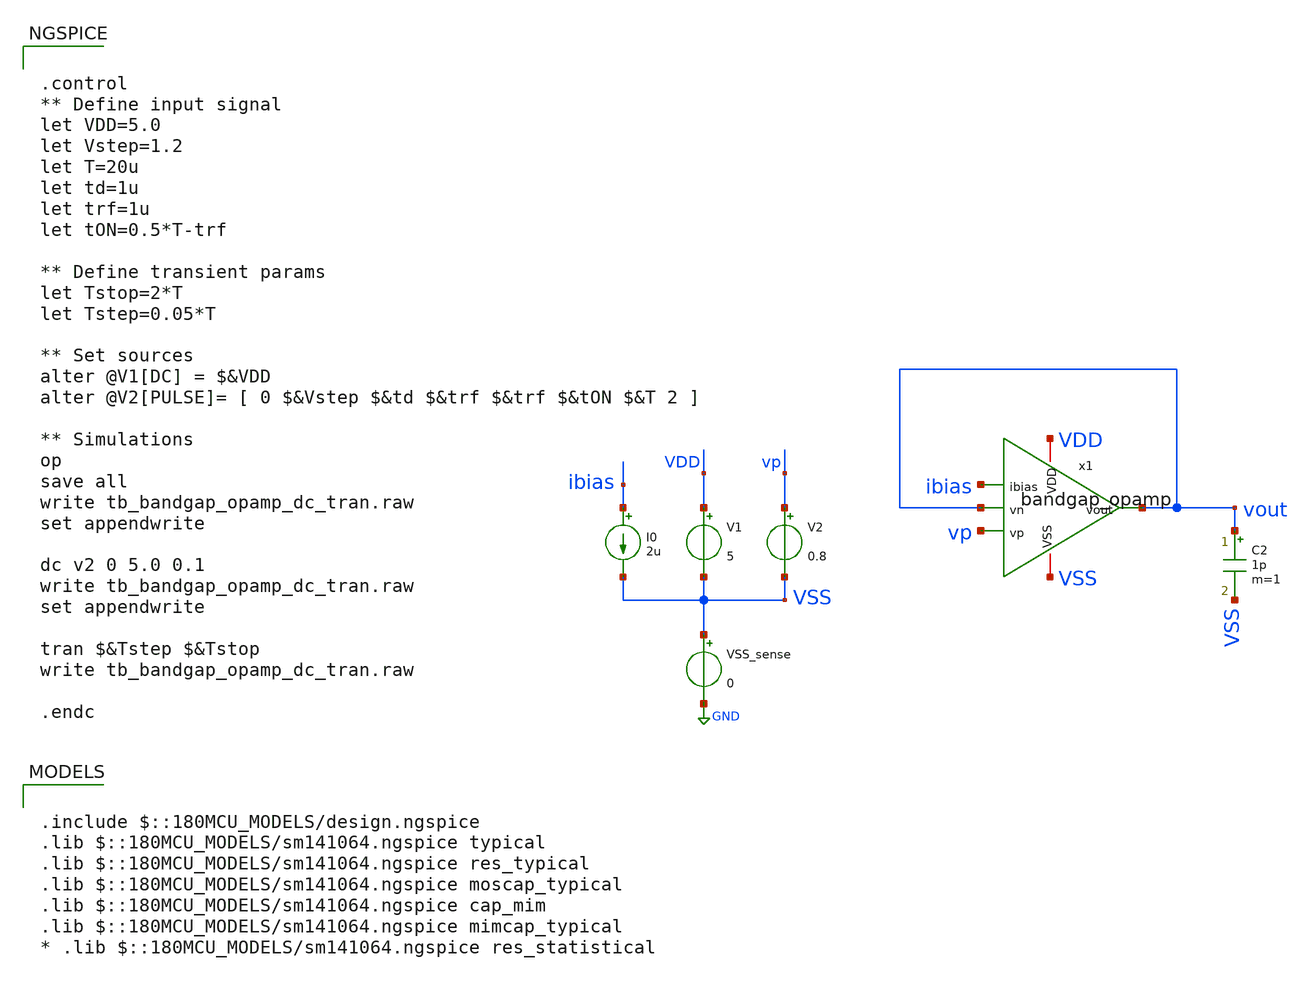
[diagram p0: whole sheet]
** sch_path: designs/libs/tb_bandgap/tb_bandgap_opamp_dc_tran/tb_bandgap_opamp_dc_tran.sch
**.subckt tb_bandgap_opamp_dc_tran
V1 VDD VSS 5
V2 vp VSS 0.8
VSS_sense VSS GND 0
C2 vout VSS 1p m=1
I0 ibias VSS 2u
x1 VDD ibias vout vp vout VSS bandgap_opamp
**** begin user architecture code

.include $::180MCU_MODELS/design.ngspice
.lib $::180MCU_MODELS/sm141064.ngspice typical
.lib $::180MCU_MODELS/sm141064.ngspice res_typical
.lib $::180MCU_MODELS/sm141064.ngspice moscap_typical
.lib $::180MCU_MODELS/sm141064.ngspice cap_mim
.lib $::180MCU_MODELS/sm141064.ngspice mimcap_typical
* .lib $::180MCU_MODELS/sm141064.ngspice res_statistical



.control
** Define input signal
let VDD=5.0
let Vstep=1.2
let T=20u
let td=1u
let trf=1u
let tON=0.5*T-trf

** Define transient params
let Tstop=2*T
let Tstep=0.05*T

** Set sources
alter @V1[DC] = $&VDD
alter @V2[PULSE]= [ 0 $&Vstep $&td $&trf $&trf $&tON $&T 2 ]

** Simulations
op
save all
write tb_bandgap_opamp_dc_tran.raw
set appendwrite

dc v2 0 5.0 0.1
write tb_bandgap_opamp_dc_tran.raw
set appendwrite

tran $&Tstep $&Tstop
write tb_bandgap_opamp_dc_tran.raw

.endc


**** end user architecture code
**.ends

* expanding   symbol:  libs/core_bandgap/bandgap_opamp/bandgap_opamp.sym # of pins=6
** sym_path: designs/libs/core_bandgap/bandgap_opamp/bandgap_opamp.sym
** sch_path: designs/libs/core_bandgap/bandgap_opamp/bandgap_opamp.sch
.subckt bandgap_opamp VDD ibias vn vp vout VSS
*.ipin vn
*.ipin vp
*.opin vout
*.ipin ibias
*.iopin VDD
*.iopin VSS
XMpref0 ibias ibias VDD VDD pfet_05v0 L=1u W=0.5u nf=1 ad='int((nf+1)/2) * W/nf * 0.18u' as='int((nf+2)/2) * W/nf * 0.18u'
+ pd='2*int((nf+1)/2) * (W/nf + 0.18u)' ps='2*int((nf+2)/2) * (W/nf + 0.18u)' nrd='0.18u / W' nrs='0.18u / W'
+ sa=0 sb=0 sd=0 m=2
XMnload0 vnload vnload VSS VSS nfet_05v0 L=2u W=0.5u nf=1 ad='int((nf+1)/2) * W/nf * 0.18u' as='int((nf+2)/2) * W/nf * 0.18u'
+ pd='2*int((nf+1)/2) * (W/nf + 0.18u)' ps='2*int((nf+2)/2) * (W/nf + 0.18u)' nrd='0.18u / W' nrs='0.18u / W'
+ sa=0 sb=0 sd=0 m=2
XMpref1 vptail ibias VDD VDD pfet_05v0 L=1u W=0.5u nf=1 ad='int((nf+1)/2) * W/nf * 0.18u' as='int((nf+2)/2) * W/nf * 0.18u'
+ pd='2*int((nf+1)/2) * (W/nf + 0.18u)' ps='2*int((nf+2)/2) * (W/nf + 0.18u)' nrd='0.18u / W' nrs='0.18u / W'
+ sa=0 sb=0 sd=0 m=2
XMpref2 vout ibias VDD VDD pfet_05v0 L=1u W=0.5u nf=1 ad='int((nf+1)/2) * W/nf * 0.18u' as='int((nf+2)/2) * W/nf * 0.18u'
+ pd='2*int((nf+1)/2) * (W/nf + 0.18u)' ps='2*int((nf+2)/2) * (W/nf + 0.18u)' nrd='0.18u / W' nrs='0.18u / W'
+ sa=0 sb=0 sd=0 m=8
XMpdiff0 vnload vn vptail VDD pfet_05v0 L=1u W=2u nf=1 ad='int((nf+1)/2) * W/nf * 0.18u' as='int((nf+2)/2) * W/nf * 0.18u'
+ pd='2*int((nf+1)/2) * (W/nf + 0.18u)' ps='2*int((nf+2)/2) * (W/nf + 0.18u)' nrd='0.18u / W' nrs='0.18u / W'
+ sa=0 sb=0 sd=0 m=2
XMpdiff1 vout_1st vp vptail VDD pfet_05v0 L=1u W=2u nf=1 ad='int((nf+1)/2) * W/nf * 0.18u' as='int((nf+2)/2) * W/nf * 0.18u'
+ pd='2*int((nf+1)/2) * (W/nf + 0.18u)' ps='2*int((nf+2)/2) * (W/nf + 0.18u)' nrd='0.18u / W' nrs='0.18u / W'
+ sa=0 sb=0 sd=0 m=2
XMnload1 vout_1st vnload VSS VSS nfet_05v0 L=2u W=0.5u nf=1 ad='int((nf+1)/2) * W/nf * 0.18u' as='int((nf+2)/2) * W/nf * 0.18u'
+ pd='2*int((nf+1)/2) * (W/nf + 0.18u)' ps='2*int((nf+2)/2) * (W/nf + 0.18u)' nrd='0.18u / W' nrs='0.18u / W'
+ sa=0 sb=0 sd=0 m=2
XMncs vout vout_1st VSS VSS nfet_05v0 L=2u W=0.5u nf=1 ad='int((nf+1)/2) * W/nf * 0.18u' as='int((nf+2)/2) * W/nf * 0.18u'
+ pd='2*int((nf+1)/2) * (W/nf + 0.18u)' ps='2*int((nf+2)/2) * (W/nf + 0.18u)' nrd='0.18u / W' nrs='0.18u / W'
+ sa=0 sb=0 sd=0 m=16
XMpref_dumm_L[3] VDD VDD VDD VDD pfet_05v0 L=1u W=0.5u nf=1 ad='int((nf+1)/2) * W/nf * 0.18u' as='int((nf+2)/2) * W/nf * 0.18u'
+ pd='2*int((nf+1)/2) * (W/nf + 0.18u)' ps='2*int((nf+2)/2) * (W/nf + 0.18u)' nrd='0.18u / W' nrs='0.18u / W'
+ sa=0 sb=0 sd=0 m=1
XMpref_dumm_L[2] VDD VDD VDD VDD pfet_05v0 L=1u W=0.5u nf=1 ad='int((nf+1)/2) * W/nf * 0.18u' as='int((nf+2)/2) * W/nf * 0.18u'
+ pd='2*int((nf+1)/2) * (W/nf + 0.18u)' ps='2*int((nf+2)/2) * (W/nf + 0.18u)' nrd='0.18u / W' nrs='0.18u / W'
+ sa=0 sb=0 sd=0 m=1
XMpref_dumm_L[1] VDD VDD VDD VDD pfet_05v0 L=1u W=0.5u nf=1 ad='int((nf+1)/2) * W/nf * 0.18u' as='int((nf+2)/2) * W/nf * 0.18u'
+ pd='2*int((nf+1)/2) * (W/nf + 0.18u)' ps='2*int((nf+2)/2) * (W/nf + 0.18u)' nrd='0.18u / W' nrs='0.18u / W'
+ sa=0 sb=0 sd=0 m=1
XMpref_dumm_L[0] VDD VDD VDD VDD pfet_05v0 L=1u W=0.5u nf=1 ad='int((nf+1)/2) * W/nf * 0.18u' as='int((nf+2)/2) * W/nf * 0.18u'
+ pd='2*int((nf+1)/2) * (W/nf + 0.18u)' ps='2*int((nf+2)/2) * (W/nf + 0.18u)' nrd='0.18u / W' nrs='0.18u / W'
+ sa=0 sb=0 sd=0 m=1
XMpref_dumm_TP[23] VDD VDD VDD VDD pfet_05v0 L=1u W=0.5u nf=1 ad='int((nf+1)/2) * W/nf * 0.18u' as='int((nf+2)/2) * W/nf * 0.18u'
+ pd='2*int((nf+1)/2) * (W/nf + 0.18u)' ps='2*int((nf+2)/2) * (W/nf + 0.18u)' nrd='0.18u / W' nrs='0.18u / W'
+ sa=0 sb=0 sd=0 m=1
XMpref_dumm_TP[22] VDD VDD VDD VDD pfet_05v0 L=1u W=0.5u nf=1 ad='int((nf+1)/2) * W/nf * 0.18u' as='int((nf+2)/2) * W/nf * 0.18u'
+ pd='2*int((nf+1)/2) * (W/nf + 0.18u)' ps='2*int((nf+2)/2) * (W/nf + 0.18u)' nrd='0.18u / W' nrs='0.18u / W'
+ sa=0 sb=0 sd=0 m=1
XMpref_dumm_TP[21] VDD VDD VDD VDD pfet_05v0 L=1u W=0.5u nf=1 ad='int((nf+1)/2) * W/nf * 0.18u' as='int((nf+2)/2) * W/nf * 0.18u'
+ pd='2*int((nf+1)/2) * (W/nf + 0.18u)' ps='2*int((nf+2)/2) * (W/nf + 0.18u)' nrd='0.18u / W' nrs='0.18u / W'
+ sa=0 sb=0 sd=0 m=1
XMpref_dumm_TP[20] VDD VDD VDD VDD pfet_05v0 L=1u W=0.5u nf=1 ad='int((nf+1)/2) * W/nf * 0.18u' as='int((nf+2)/2) * W/nf * 0.18u'
+ pd='2*int((nf+1)/2) * (W/nf + 0.18u)' ps='2*int((nf+2)/2) * (W/nf + 0.18u)' nrd='0.18u / W' nrs='0.18u / W'
+ sa=0 sb=0 sd=0 m=1
XMpref_dumm_TP[19] VDD VDD VDD VDD pfet_05v0 L=1u W=0.5u nf=1 ad='int((nf+1)/2) * W/nf * 0.18u' as='int((nf+2)/2) * W/nf * 0.18u'
+ pd='2*int((nf+1)/2) * (W/nf + 0.18u)' ps='2*int((nf+2)/2) * (W/nf + 0.18u)' nrd='0.18u / W' nrs='0.18u / W'
+ sa=0 sb=0 sd=0 m=1
XMpref_dumm_TP[18] VDD VDD VDD VDD pfet_05v0 L=1u W=0.5u nf=1 ad='int((nf+1)/2) * W/nf * 0.18u' as='int((nf+2)/2) * W/nf * 0.18u'
+ pd='2*int((nf+1)/2) * (W/nf + 0.18u)' ps='2*int((nf+2)/2) * (W/nf + 0.18u)' nrd='0.18u / W' nrs='0.18u / W'
+ sa=0 sb=0 sd=0 m=1
XMpref_dumm_TP[17] VDD VDD VDD VDD pfet_05v0 L=1u W=0.5u nf=1 ad='int((nf+1)/2) * W/nf * 0.18u' as='int((nf+2)/2) * W/nf * 0.18u'
+ pd='2*int((nf+1)/2) * (W/nf + 0.18u)' ps='2*int((nf+2)/2) * (W/nf + 0.18u)' nrd='0.18u / W' nrs='0.18u / W'
+ sa=0 sb=0 sd=0 m=1
XMpref_dumm_TP[16] VDD VDD VDD VDD pfet_05v0 L=1u W=0.5u nf=1 ad='int((nf+1)/2) * W/nf * 0.18u' as='int((nf+2)/2) * W/nf * 0.18u'
+ pd='2*int((nf+1)/2) * (W/nf + 0.18u)' ps='2*int((nf+2)/2) * (W/nf + 0.18u)' nrd='0.18u / W' nrs='0.18u / W'
+ sa=0 sb=0 sd=0 m=1
XMpref_dumm_TP[15] VDD VDD VDD VDD pfet_05v0 L=1u W=0.5u nf=1 ad='int((nf+1)/2) * W/nf * 0.18u' as='int((nf+2)/2) * W/nf * 0.18u'
+ pd='2*int((nf+1)/2) * (W/nf + 0.18u)' ps='2*int((nf+2)/2) * (W/nf + 0.18u)' nrd='0.18u / W' nrs='0.18u / W'
+ sa=0 sb=0 sd=0 m=1
XMpref_dumm_TP[14] VDD VDD VDD VDD pfet_05v0 L=1u W=0.5u nf=1 ad='int((nf+1)/2) * W/nf * 0.18u' as='int((nf+2)/2) * W/nf * 0.18u'
+ pd='2*int((nf+1)/2) * (W/nf + 0.18u)' ps='2*int((nf+2)/2) * (W/nf + 0.18u)' nrd='0.18u / W' nrs='0.18u / W'
+ sa=0 sb=0 sd=0 m=1
XMpref_dumm_TP[13] VDD VDD VDD VDD pfet_05v0 L=1u W=0.5u nf=1 ad='int((nf+1)/2) * W/nf * 0.18u' as='int((nf+2)/2) * W/nf * 0.18u'
+ pd='2*int((nf+1)/2) * (W/nf + 0.18u)' ps='2*int((nf+2)/2) * (W/nf + 0.18u)' nrd='0.18u / W' nrs='0.18u / W'
+ sa=0 sb=0 sd=0 m=1
XMpref_dumm_TP[12] VDD VDD VDD VDD pfet_05v0 L=1u W=0.5u nf=1 ad='int((nf+1)/2) * W/nf * 0.18u' as='int((nf+2)/2) * W/nf * 0.18u'
+ pd='2*int((nf+1)/2) * (W/nf + 0.18u)' ps='2*int((nf+2)/2) * (W/nf + 0.18u)' nrd='0.18u / W' nrs='0.18u / W'
+ sa=0 sb=0 sd=0 m=1
XMpref_dumm_TP[11] VDD VDD VDD VDD pfet_05v0 L=1u W=0.5u nf=1 ad='int((nf+1)/2) * W/nf * 0.18u' as='int((nf+2)/2) * W/nf * 0.18u'
+ pd='2*int((nf+1)/2) * (W/nf + 0.18u)' ps='2*int((nf+2)/2) * (W/nf + 0.18u)' nrd='0.18u / W' nrs='0.18u / W'
+ sa=0 sb=0 sd=0 m=1
XMpref_dumm_TP[10] VDD VDD VDD VDD pfet_05v0 L=1u W=0.5u nf=1 ad='int((nf+1)/2) * W/nf * 0.18u' as='int((nf+2)/2) * W/nf * 0.18u'
+ pd='2*int((nf+1)/2) * (W/nf + 0.18u)' ps='2*int((nf+2)/2) * (W/nf + 0.18u)' nrd='0.18u / W' nrs='0.18u / W'
+ sa=0 sb=0 sd=0 m=1
XMpref_dumm_TP[9] VDD VDD VDD VDD pfet_05v0 L=1u W=0.5u nf=1 ad='int((nf+1)/2) * W/nf * 0.18u' as='int((nf+2)/2) * W/nf * 0.18u'
+ pd='2*int((nf+1)/2) * (W/nf + 0.18u)' ps='2*int((nf+2)/2) * (W/nf + 0.18u)' nrd='0.18u / W' nrs='0.18u / W'
+ sa=0 sb=0 sd=0 m=1
XMpref_dumm_TP[8] VDD VDD VDD VDD pfet_05v0 L=1u W=0.5u nf=1 ad='int((nf+1)/2) * W/nf * 0.18u' as='int((nf+2)/2) * W/nf * 0.18u'
+ pd='2*int((nf+1)/2) * (W/nf + 0.18u)' ps='2*int((nf+2)/2) * (W/nf + 0.18u)' nrd='0.18u / W' nrs='0.18u / W'
+ sa=0 sb=0 sd=0 m=1
XMpref_dumm_TP[7] VDD VDD VDD VDD pfet_05v0 L=1u W=0.5u nf=1 ad='int((nf+1)/2) * W/nf * 0.18u' as='int((nf+2)/2) * W/nf * 0.18u'
+ pd='2*int((nf+1)/2) * (W/nf + 0.18u)' ps='2*int((nf+2)/2) * (W/nf + 0.18u)' nrd='0.18u / W' nrs='0.18u / W'
+ sa=0 sb=0 sd=0 m=1
XMpref_dumm_TP[6] VDD VDD VDD VDD pfet_05v0 L=1u W=0.5u nf=1 ad='int((nf+1)/2) * W/nf * 0.18u' as='int((nf+2)/2) * W/nf * 0.18u'
+ pd='2*int((nf+1)/2) * (W/nf + 0.18u)' ps='2*int((nf+2)/2) * (W/nf + 0.18u)' nrd='0.18u / W' nrs='0.18u / W'
+ sa=0 sb=0 sd=0 m=1
XMpref_dumm_TP[5] VDD VDD VDD VDD pfet_05v0 L=1u W=0.5u nf=1 ad='int((nf+1)/2) * W/nf * 0.18u' as='int((nf+2)/2) * W/nf * 0.18u'
+ pd='2*int((nf+1)/2) * (W/nf + 0.18u)' ps='2*int((nf+2)/2) * (W/nf + 0.18u)' nrd='0.18u / W' nrs='0.18u / W'
+ sa=0 sb=0 sd=0 m=1
XMpref_dumm_TP[4] VDD VDD VDD VDD pfet_05v0 L=1u W=0.5u nf=1 ad='int((nf+1)/2) * W/nf * 0.18u' as='int((nf+2)/2) * W/nf * 0.18u'
+ pd='2*int((nf+1)/2) * (W/nf + 0.18u)' ps='2*int((nf+2)/2) * (W/nf + 0.18u)' nrd='0.18u / W' nrs='0.18u / W'
+ sa=0 sb=0 sd=0 m=1
XMpref_dumm_TP[3] VDD VDD VDD VDD pfet_05v0 L=1u W=0.5u nf=1 ad='int((nf+1)/2) * W/nf * 0.18u' as='int((nf+2)/2) * W/nf * 0.18u'
+ pd='2*int((nf+1)/2) * (W/nf + 0.18u)' ps='2*int((nf+2)/2) * (W/nf + 0.18u)' nrd='0.18u / W' nrs='0.18u / W'
+ sa=0 sb=0 sd=0 m=1
XMpref_dumm_TP[2] VDD VDD VDD VDD pfet_05v0 L=1u W=0.5u nf=1 ad='int((nf+1)/2) * W/nf * 0.18u' as='int((nf+2)/2) * W/nf * 0.18u'
+ pd='2*int((nf+1)/2) * (W/nf + 0.18u)' ps='2*int((nf+2)/2) * (W/nf + 0.18u)' nrd='0.18u / W' nrs='0.18u / W'
+ sa=0 sb=0 sd=0 m=1
XMpref_dumm_TP[1] VDD VDD VDD VDD pfet_05v0 L=1u W=0.5u nf=1 ad='int((nf+1)/2) * W/nf * 0.18u' as='int((nf+2)/2) * W/nf * 0.18u'
+ pd='2*int((nf+1)/2) * (W/nf + 0.18u)' ps='2*int((nf+2)/2) * (W/nf + 0.18u)' nrd='0.18u / W' nrs='0.18u / W'
+ sa=0 sb=0 sd=0 m=1
XMpref_dumm_TP[0] VDD VDD VDD VDD pfet_05v0 L=1u W=0.5u nf=1 ad='int((nf+1)/2) * W/nf * 0.18u' as='int((nf+2)/2) * W/nf * 0.18u'
+ pd='2*int((nf+1)/2) * (W/nf + 0.18u)' ps='2*int((nf+2)/2) * (W/nf + 0.18u)' nrd='0.18u / W' nrs='0.18u / W'
+ sa=0 sb=0 sd=0 m=1
XC1[5] vout vout_1st cap_mim_1f0fF c_width=10e-6 c_length=10e-6 m=1
XC1[4] vout vout_1st cap_mim_1f0fF c_width=10e-6 c_length=10e-6 m=1
XC1[3] vout vout_1st cap_mim_1f0fF c_width=10e-6 c_length=10e-6 m=1
XC1[2] vout vout_1st cap_mim_1f0fF c_width=10e-6 c_length=10e-6 m=1
XC1[1] vout vout_1st cap_mim_1f0fF c_width=10e-6 c_length=10e-6 m=1
XC1[0] vout vout_1st cap_mim_1f0fF c_width=10e-6 c_length=10e-6 m=1
.ends

.GLOBAL GND
.end
